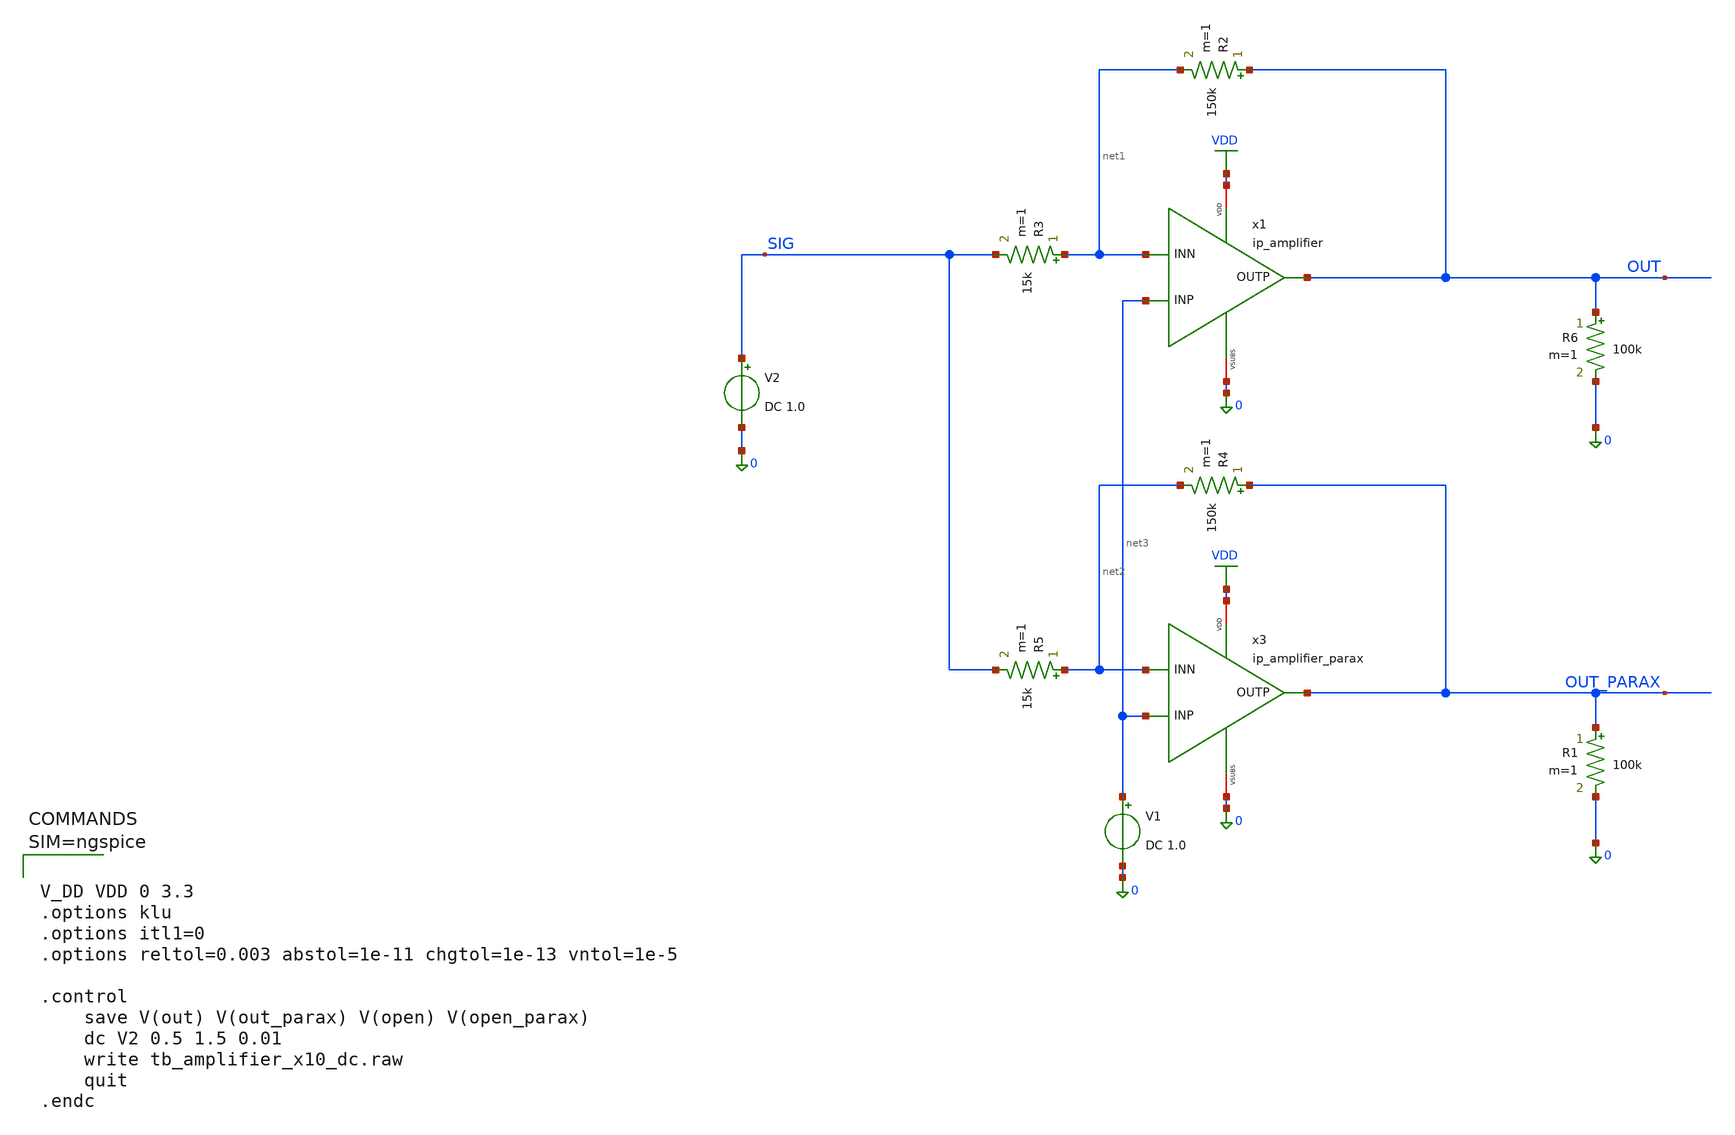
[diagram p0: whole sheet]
** sch_path: xschem/tb_amplifier_x10_dc.sch
**.subckt tb_amplifier_x10_dc
x1 VDD OUT net3 net1 0 ip_amplifier
R6 OUT 0 100k m=1
V2 SIG 0 DC 1.0
R1 OUT_PARAX 0 100k m=1
x3 VDD OUT_PARAX net3 net2 0 ip_amplifier_parax
R2 OUT net1 150k m=1
R3 net1 SIG 15k m=1
R4 OUT_PARAX net2 150k m=1
R5 net2 SIG 15k m=1
V1 net3 0 DC 1.0
**** begin user architecture code

.inc $::180MCU_MODELS/design.spice
.lib $::180MCU_MODELS/sm141064.ngspice typical
.lib $::180MCU_MODELS/sm141064.ngspice moscap_typical
.lib $::180MCU_MODELS/sm141064.ngspice diode_typical
.lib $::180MCU_MODELS/sm141064.ngspice res_typical




V_DD VDD 0 3.3
.options klu
.options itl1=0
.options reltol=0.003 abstol=1e-11 chgtol=1e-13 vntol=1e-5

.control
	save V(out) V(out_parax) V(open) V(open_parax)
	dc V2 0.5 1.5 0.01
	write tb_amplifier_x10_dc.raw
	quit
.endc



**** end user architecture code
**.ends

* expanding   symbol:  ip_amplifier.sym # of pins=5
** sym_path: xschem/ip_amplifier.sym
** sch_path: xschem/ip_amplifier.sch
.subckt ip_amplifier VDD OUTP INP INN VSUBS
*.iopin VDD
*.iopin VSUBS
*.ipin INP
*.ipin INN
*.opin OUTP
XM1 net10 INP net8 VDD pfet_06v0 L=0.7u W=11.0u nf=1 ad='int((nf+1)/2) * W/nf * 0.18u' as='int((nf+2)/2) * W/nf * 0.18u'
+ pd='2*int((nf+1)/2) * (W/nf + 0.18u)' ps='2*int((nf+2)/2) * (W/nf + 0.18u)' nrd='0.18u / W' nrs='0.18u / W'
+ sa=0 sb=0 sd=0 m=2 par=2
XM2 net9 INN net8 VDD pfet_06v0 L=0.7u W=11.0u nf=1 ad='int((nf+1)/2) * W/nf * 0.18u' as='int((nf+2)/2) * W/nf * 0.18u'
+ pd='2*int((nf+1)/2) * (W/nf + 0.18u)' ps='2*int((nf+2)/2) * (W/nf + 0.18u)' nrd='0.18u / W' nrs='0.18u / W'
+ sa=0 sb=0 sd=0 m=2 par=2
XM5 net10 net1 VSUBS vsubs nfet_06v0 L=2u W=5u nf=1 ad='int((nf+1)/2) * W/nf * 0.18u' as='int((nf+2)/2) * W/nf * 0.18u'
+ pd='2*int((nf+1)/2) * (W/nf + 0.18u)' ps='2*int((nf+2)/2) * (W/nf + 0.18u)' nrd='0.18u / W' nrs='0.18u / W'
+ sa=0 sb=0 sd=0 m=1 par=1
XM6 net9 net1 VSUBS vsubs nfet_06v0 L=2u W=5u nf=1 ad='int((nf+1)/2) * W/nf * 0.18u' as='int((nf+2)/2) * W/nf * 0.18u'
+ pd='2*int((nf+1)/2) * (W/nf + 0.18u)' ps='2*int((nf+2)/2) * (W/nf + 0.18u)' nrd='0.18u / W' nrs='0.18u / W'
+ sa=0 sb=0 sd=0 m=1 par=1
XM3 net3 net1 VSUBS vsubs nfet_06v0 L=1u W=12.5u nf=1 ad='int((nf+1)/2) * W/nf * 0.18u' as='int((nf+2)/2) * W/nf * 0.18u'
+ pd='2*int((nf+1)/2) * (W/nf + 0.18u)' ps='2*int((nf+2)/2) * (W/nf + 0.18u)' nrd='0.18u / W' nrs='0.18u / W'
+ sa=0 sb=0 sd=0 m=2 par=2
XM4 net2 net1 VSUBS vsubs nfet_06v0 L=1u W=5u nf=1 ad='int((nf+1)/2) * W/nf * 0.18u' as='int((nf+2)/2) * W/nf * 0.18u'
+ pd='2*int((nf+1)/2) * (W/nf + 0.18u)' ps='2*int((nf+2)/2) * (W/nf + 0.18u)' nrd='0.18u / W' nrs='0.18u / W'
+ sa=0 sb=0 sd=0 m=1 par=1
XM7 net1 net1 net3 vsubs nfet_06v0 L=0.7u W=14u nf=1 ad='int((nf+1)/2) * W/nf * 0.18u' as='int((nf+2)/2) * W/nf * 0.18u'
+ pd='2*int((nf+1)/2) * (W/nf + 0.18u)' ps='2*int((nf+2)/2) * (W/nf + 0.18u)' nrd='0.18u / W' nrs='0.18u / W'
+ sa=0 sb=0 sd=0 m=2 par=2
XM8 net4 net1 net2 vsubs nfet_06v0 L=0.7u W=14u nf=1 ad='int((nf+1)/2) * W/nf * 0.18u' as='int((nf+2)/2) * W/nf * 0.18u'
+ pd='2*int((nf+1)/2) * (W/nf + 0.18u)' ps='2*int((nf+2)/2) * (W/nf + 0.18u)' nrd='0.18u / W' nrs='0.18u / W'
+ sa=0 sb=0 sd=0 m=2 par=2
XM9 net5 net7 VDD VDD pfet_06v0 L=1u W=6u nf=1 ad='int((nf+1)/2) * W/nf * 0.18u' as='int((nf+2)/2) * W/nf * 0.18u'
+ pd='2*int((nf+1)/2) * (W/nf + 0.18u)' ps='2*int((nf+2)/2) * (W/nf + 0.18u)' nrd='0.18u / W' nrs='0.18u / W'
+ sa=0 sb=0 sd=0 m=1 par=1
XM10 net6 net7 VDD VDD pfet_06v0 L=1u W=6u nf=1 ad='int((nf+1)/2) * W/nf * 0.18u' as='int((nf+2)/2) * W/nf * 0.18u'
+ pd='2*int((nf+1)/2) * (W/nf + 0.18u)' ps='2*int((nf+2)/2) * (W/nf + 0.18u)' nrd='0.18u / W' nrs='0.18u / W'
+ sa=0 sb=0 sd=0 m=1 par=1
XM11 net7 net7 net5 VDD pfet_06v0 L=0.7u W=14u nf=1 ad='int((nf+1)/2) * W/nf * 0.18u' as='int((nf+2)/2) * W/nf * 0.18u'
+ pd='2*int((nf+1)/2) * (W/nf + 0.18u)' ps='2*int((nf+2)/2) * (W/nf + 0.18u)' nrd='0.18u / W' nrs='0.18u / W'
+ sa=0 sb=0 sd=0 m=2 par=2
XM12 net8 net7 net6 VDD pfet_06v0 L=0.7u W=14u nf=1 ad='int((nf+1)/2) * W/nf * 0.18u' as='int((nf+2)/2) * W/nf * 0.18u'
+ pd='2*int((nf+1)/2) * (W/nf + 0.18u)' ps='2*int((nf+2)/2) * (W/nf + 0.18u)' nrd='0.18u / W' nrs='0.18u / W'
+ sa=0 sb=0 sd=0 m=2 par=2
XM13 net11 net1 net9 vsubs nfet_06v0 L=0.7u W=12u nf=1 ad='int((nf+1)/2) * W/nf * 0.18u' as='int((nf+2)/2) * W/nf * 0.18u'
+ pd='2*int((nf+1)/2) * (W/nf + 0.18u)' ps='2*int((nf+2)/2) * (W/nf + 0.18u)' nrd='0.18u / W' nrs='0.18u / W'
+ sa=0 sb=0 sd=0 m=1 par=1
XM14 COMP net1 net10 vsubs nfet_06v0 L=0.7u W=12u nf=1 ad='int((nf+1)/2) * W/nf * 0.18u' as='int((nf+2)/2) * W/nf * 0.18u'
+ pd='2*int((nf+1)/2) * (W/nf + 0.18u)' ps='2*int((nf+2)/2) * (W/nf + 0.18u)' nrd='0.18u / W' nrs='0.18u / W'
+ sa=0 sb=0 sd=0 m=1 par=1
XM15 net11 net11 VDD VDD pfet_06v0 L=0.7u W=12u nf=1 ad='int((nf+1)/2) * W/nf * 0.18u' as='int((nf+2)/2) * W/nf * 0.18u'
+ pd='2*int((nf+1)/2) * (W/nf + 0.18u)' ps='2*int((nf+2)/2) * (W/nf + 0.18u)' nrd='0.18u / W' nrs='0.18u / W'
+ sa=0 sb=0 sd=0 m=1 par=1
XM16 COMP net11 VDD VDD pfet_06v0 L=0.7u W=12u nf=1 ad='int((nf+1)/2) * W/nf * 0.18u' as='int((nf+2)/2) * W/nf * 0.18u'
+ pd='2*int((nf+1)/2) * (W/nf + 0.18u)' ps='2*int((nf+2)/2) * (W/nf + 0.18u)' nrd='0.18u / W' nrs='0.18u / W'
+ sa=0 sb=0 sd=0 m=1 par=1
XM17 OUTP COMP VDD VDD pfet_06v0 L=0.7u W=12u nf=1 ad='int((nf+1)/2) * W/nf * 0.18u' as='int((nf+2)/2) * W/nf * 0.18u'
+ pd='2*int((nf+1)/2) * (W/nf + 0.18u)' ps='2*int((nf+2)/2) * (W/nf + 0.18u)' nrd='0.18u / W' nrs='0.18u / W'
+ sa=0 sb=0 sd=0 m=5 par=5
XM18 OUTP net10 VSUBS vsubs nfet_06v0 L=0.7u W=12u nf=1 ad='int((nf+1)/2) * W/nf * 0.18u' as='int((nf+2)/2) * W/nf * 0.18u'
+ pd='2*int((nf+1)/2) * (W/nf + 0.18u)' ps='2*int((nf+2)/2) * (W/nf + 0.18u)' nrd='0.18u / W' nrs='0.18u / W'
+ sa=0 sb=0 sd=0 m=3 par=3
XR3 net1 net14 vsubs ppolyf_u_1k_6p0 r_width=1e-6 r_length=6e-6 m=1
XR6 net14 net13 vsubs ppolyf_u_1k_6p0 r_width=1e-6 r_length=6e-6 m=1
XR7 net13 net12 vsubs ppolyf_u_1k_6p0 r_width=1e-6 r_length=6e-6 m=1
XR8 net12 net15 vsubs ppolyf_u_1k_6p0 r_width=1e-6 r_length=4e-6 m=1
Vmeas VDD net15 0
Vmeas1 net7 net4 0
XC1 OUTP net16 cap_nmos_03v3 c_width=12e-6 c_length=18e-6 m=1
XC2 COMP net17 cap_nmos_03v3 c_width=12e-6 c_length=18e-6 m=1
XR12 net16 COMP vsubs ppolyf_u_1k_6p0 r_width=1e-6 r_length=10e-6 m=1
XR16 OUTP net17 vsubs ppolyf_u_1k_6p0 r_width=1e-6 r_length=10e-6 m=1
.ends


* expanding   symbol:  ip_amplifier_parax.sym # of pins=5
** sym_path: xschem/ip_amplifier.sym
.include [file normalize ./parax/ip_amplifier.sim.spice]
.GLOBAL VDD
.end
